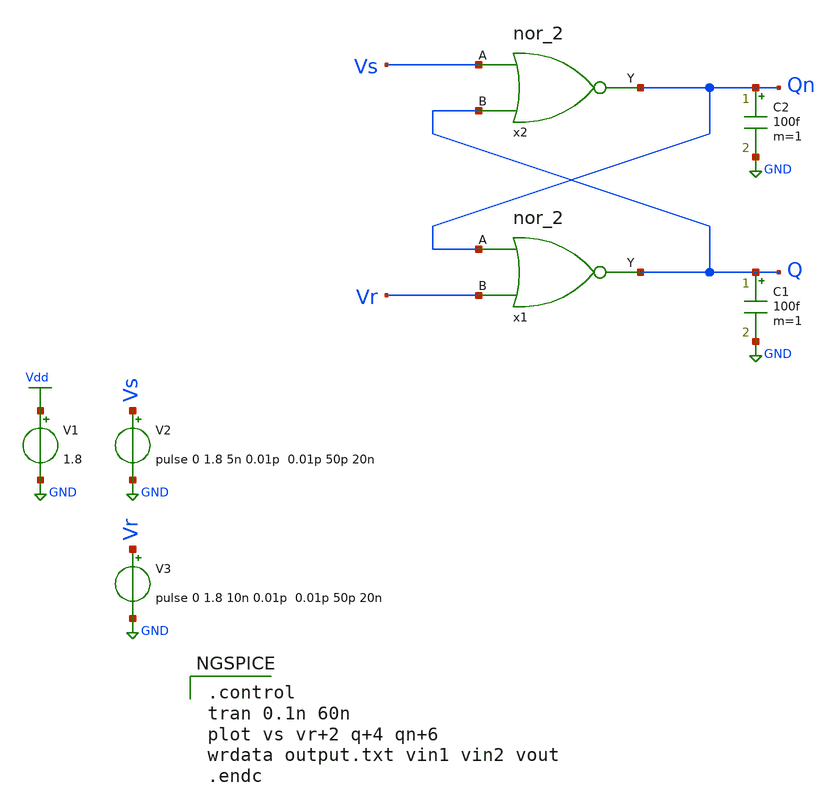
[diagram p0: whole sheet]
** sch_path: Circuiti/sr_latch.sch
**.subckt sr_latch
x1 Qn Q Vr nor_2
x2 Vs Qn Q nor_2
V1 Vdd GND 1.8
V2 Vs GND pulse 0 1.8 5n 0.01p 0.01p 50p 20n
V3 Vr GND pulse 0 1.8 10n 0.01p 0.01p 50p 20n
C1 Q GND 100f m=1
C2 Qn GND 100f m=1
**** begin user architecture code


.lib /home/matteo/xschem_downloads/skywater-pdk/libraries/sky130_fd_pr_ngspice/latest/models/sky130.lib.spice tt

*.include /home/matteo/xschem_downloads/skywater-pdk/libraries/sky130_fd_pr_ngspice/latest/cells/nfet_01v8/sky130_fd_pr__nfet_01v8__tt.corner.spice

.param mc_mm_switch=0
.param mc_pr_switch=1



.control
tran 0.1n 60n
plot vs vr+2 q+4 qn+6
wrdata output.txt vin1 vin2 vout
.endc


**** end user architecture code
**.ends

* expanding   symbol:  /home/matteo/Documenti/tesi/Circuiti/logic_gates_sch_sym/nor_2.sym # of
*+ pins=3
** sym_path: Circuiti/logic_gates_sch_sym/nor_2.sym
** sch_path: Circuiti/logic_gates_sch_sym/nor_2.sch
.subckt nor_2 A Y B
*.opin Y
*.ipin A
*.ipin B
XM1 Y B GND GND sky130_fd_pr__nfet_01v8 L=0.45 W=1 nf=1 ad='int((nf+1)/2) * W/nf * 0.29' as='int((nf+2)/2) * W/nf * 0.29'
+ pd='2*int((nf+1)/2) * (W/nf + 0.29)' ps='2*int((nf+2)/2) * (W/nf + 0.29)' nrd='0.29 / W' nrs='0.29 / W'
+ sa=0 sb=0 sd=0 mult=1 m=1
XM3 Y B net1 VDD sky130_fd_pr__pfet_01v8 L=0.15 W=4.8 nf=1 ad='int((nf+1)/2) * W/nf * 0.29' as='int((nf+2)/2) * W/nf * 0.29'
+ pd='2*int((nf+1)/2) * (W/nf + 0.29)' ps='2*int((nf+2)/2) * (W/nf + 0.29)' nrd='0.29 / W' nrs='0.29 / W'
+ sa=0 sb=0 sd=0 mult=1 m=1
XM4 net1 A Vdd VDD sky130_fd_pr__pfet_01v8 L=0.15 W=4.8 nf=1 ad='int((nf+1)/2) * W/nf * 0.29' as='int((nf+2)/2) * W/nf * 0.29'
+ pd='2*int((nf+1)/2) * (W/nf + 0.29)' ps='2*int((nf+2)/2) * (W/nf + 0.29)' nrd='0.29 / W' nrs='0.29 / W'
+ sa=0 sb=0 sd=0 mult=1 m=1
XM2 Y A GND GND sky130_fd_pr__nfet_01v8 L=0.45 W=1 nf=1 ad='int((nf+1)/2) * W/nf * 0.29' as='int((nf+2)/2) * W/nf * 0.29'
+ pd='2*int((nf+1)/2) * (W/nf + 0.29)' ps='2*int((nf+2)/2) * (W/nf + 0.29)' nrd='0.29 / W' nrs='0.29 / W'
+ sa=0 sb=0 sd=0 mult=1 m=1
.ends

.GLOBAL GND
.GLOBAL Vdd
.end
